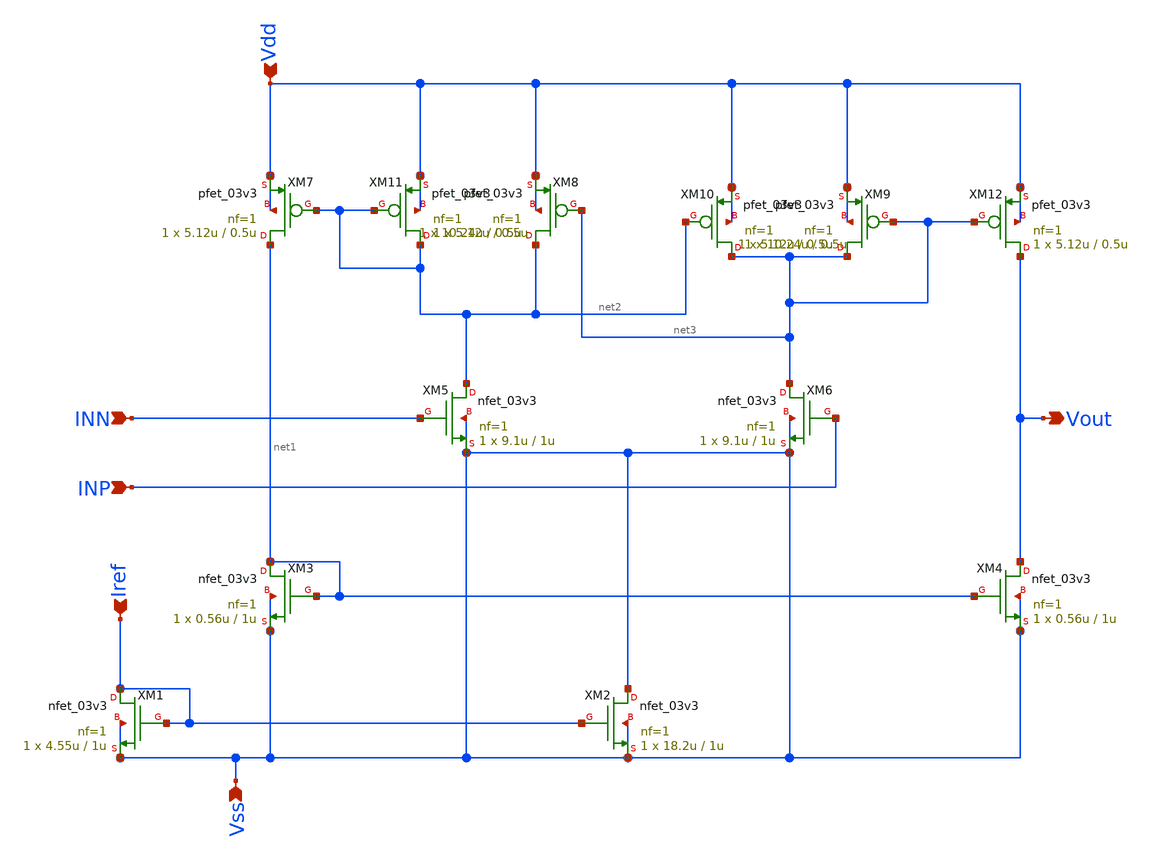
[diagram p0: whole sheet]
** sch_path: designs/libs/core_analog/Comparator/Nmos_Comparator.sch
**.subckt Nmos_Comparator Vss Vdd Iref INN INP Vout
*.ipin Vss
*.ipin Vdd
*.ipin Iref
*.ipin INN
*.ipin INP
*.opin Vout
XM1 Iref Iref Vss Vss nfet_03v3 L=1u W=4.55u nf=1 ad='int((nf+1)/2) * W/nf * 0.18u' as='int((nf+2)/2) * W/nf * 0.18u'
+ pd='2*int((nf+1)/2) * (W/nf + 0.18u)' ps='2*int((nf+2)/2) * (W/nf + 0.18u)' nrd='0.18u / W' nrs='0.18u / W'
+ sa=0 sb=0 sd=0 m=1
XM2 Vss Iref Vss Vss nfet_03v3 L=1u W=18.2u nf=1 ad='int((nf+1)/2) * W/nf * 0.18u' as='int((nf+2)/2) * W/nf * 0.18u'
+ pd='2*int((nf+1)/2) * (W/nf + 0.18u)' ps='2*int((nf+2)/2) * (W/nf + 0.18u)' nrd='0.18u / W' nrs='0.18u / W'
+ sa=0 sb=0 sd=0 m=1
XM3 net1 net1 Vss Vss nfet_03v3 L=1u W=0.56u nf=1 ad='int((nf+1)/2) * W/nf * 0.18u' as='int((nf+2)/2) * W/nf * 0.18u'
+ pd='2*int((nf+1)/2) * (W/nf + 0.18u)' ps='2*int((nf+2)/2) * (W/nf + 0.18u)' nrd='0.18u / W' nrs='0.18u / W'
+ sa=0 sb=0 sd=0 m=1
XM4 Vout net1 Vss Vss nfet_03v3 L=1u W=0.56u nf=1 ad='int((nf+1)/2) * W/nf * 0.18u' as='int((nf+2)/2) * W/nf * 0.18u'
+ pd='2*int((nf+1)/2) * (W/nf + 0.18u)' ps='2*int((nf+2)/2) * (W/nf + 0.18u)' nrd='0.18u / W' nrs='0.18u / W'
+ sa=0 sb=0 sd=0 m=1
XM5 net2 INN Vss Vss nfet_03v3 L=1u W=9.1u nf=1 ad='int((nf+1)/2) * W/nf * 0.18u' as='int((nf+2)/2) * W/nf * 0.18u'
+ pd='2*int((nf+1)/2) * (W/nf + 0.18u)' ps='2*int((nf+2)/2) * (W/nf + 0.18u)' nrd='0.18u / W' nrs='0.18u / W'
+ sa=0 sb=0 sd=0 m=1
XM6 net3 INP Vss Vss nfet_03v3 L=1u W=9.1u nf=1 ad='int((nf+1)/2) * W/nf * 0.18u' as='int((nf+2)/2) * W/nf * 0.18u'
+ pd='2*int((nf+1)/2) * (W/nf + 0.18u)' ps='2*int((nf+2)/2) * (W/nf + 0.18u)' nrd='0.18u / W' nrs='0.18u / W'
+ sa=0 sb=0 sd=0 m=1
XM7 net1 net2 Vdd Vdd pfet_03v3 L=0.5u W=5.12u nf=1 ad='int((nf+1)/2) * W/nf * 0.18u' as='int((nf+2)/2) * W/nf * 0.18u'
+ pd='2*int((nf+1)/2) * (W/nf + 0.18u)' ps='2*int((nf+2)/2) * (W/nf + 0.18u)' nrd='0.18u / W' nrs='0.18u / W'
+ sa=0 sb=0 sd=0 m=1
XM8 net2 net3 Vdd Vdd pfet_03v3 L=0.5u W=10.24u nf=1 ad='int((nf+1)/2) * W/nf * 0.18u' as='int((nf+2)/2) * W/nf * 0.18u'
+ pd='2*int((nf+1)/2) * (W/nf + 0.18u)' ps='2*int((nf+2)/2) * (W/nf + 0.18u)' nrd='0.18u / W' nrs='0.18u / W'
+ sa=0 sb=0 sd=0 m=1
XM9 net3 net3 Vdd Vdd pfet_03v3 L=0.5u W=5.12u nf=1 ad='int((nf+1)/2) * W/nf * 0.18u' as='int((nf+2)/2) * W/nf * 0.18u'
+ pd='2*int((nf+1)/2) * (W/nf + 0.18u)' ps='2*int((nf+2)/2) * (W/nf + 0.18u)' nrd='0.18u / W' nrs='0.18u / W'
+ sa=0 sb=0 sd=0 m=1
XM10 net3 net2 Vdd Vdd pfet_03v3 L=0.5u W=10.24u nf=1 ad='int((nf+1)/2) * W/nf * 0.18u' as='int((nf+2)/2) * W/nf * 0.18u'
+ pd='2*int((nf+1)/2) * (W/nf + 0.18u)' ps='2*int((nf+2)/2) * (W/nf + 0.18u)' nrd='0.18u / W' nrs='0.18u / W'
+ sa=0 sb=0 sd=0 m=1
XM11 net2 net2 Vdd Vdd pfet_03v3 L=0.5u W=5.12u nf=1 ad='int((nf+1)/2) * W/nf * 0.18u' as='int((nf+2)/2) * W/nf * 0.18u'
+ pd='2*int((nf+1)/2) * (W/nf + 0.18u)' ps='2*int((nf+2)/2) * (W/nf + 0.18u)' nrd='0.18u / W' nrs='0.18u / W'
+ sa=0 sb=0 sd=0 m=1
XM12 Vout net3 Vdd Vdd pfet_03v3 L=0.5u W=5.12u nf=1 ad='int((nf+1)/2) * W/nf * 0.18u' as='int((nf+2)/2) * W/nf * 0.18u'
+ pd='2*int((nf+1)/2) * (W/nf + 0.18u)' ps='2*int((nf+2)/2) * (W/nf + 0.18u)' nrd='0.18u / W' nrs='0.18u / W'
+ sa=0 sb=0 sd=0 m=1
**.ends
.end
